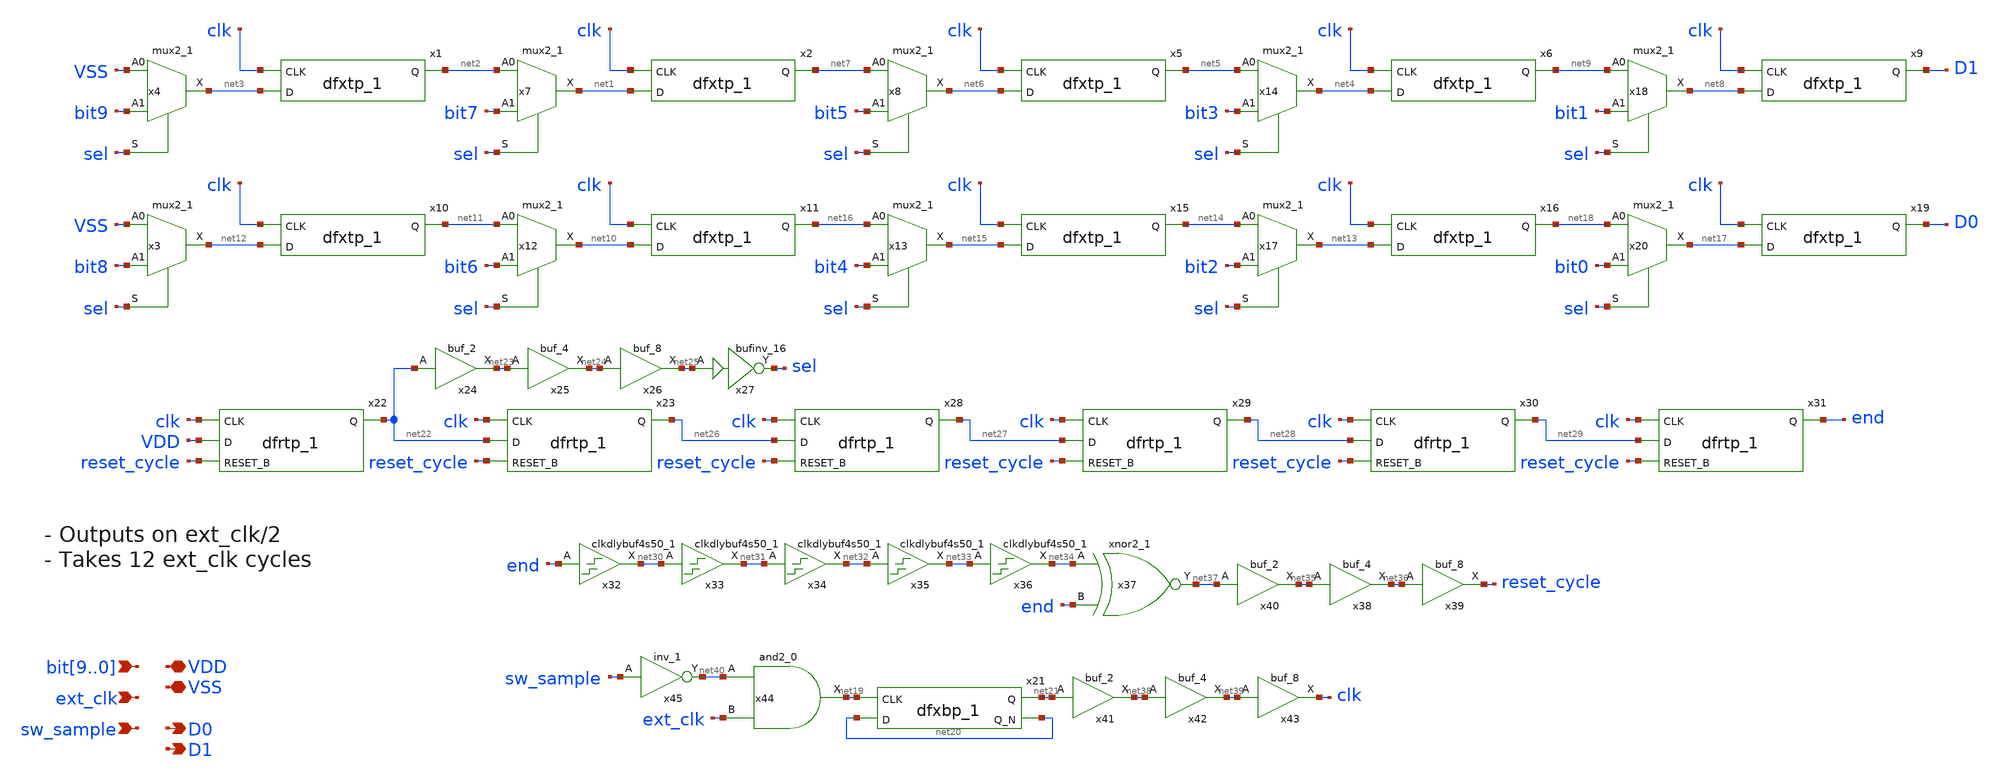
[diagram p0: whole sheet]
** sch_path: xschem/src/serializer/serializer.sch
**.subckt serializer bit9,bit8,bit7,bit6,bit5,bit4,bit3,bit2,bit1,bit0 VDD D0 VSS D1 ext_clk
*+ sw_sample
*.ipin bit9,bit8,bit7,bit6,bit5,bit4,bit3,bit2,bit1,bit0
*.iopin VDD
*.opin D0
*.iopin VSS
*.opin D1
*.ipin ext_clk
*.ipin sw_sample
x1 clk net3 VSS VSS VDD VDD net2 sky130_fd_sc_hd__dfxtp_1
x2 clk net1 VSS VSS VDD VDD net7 sky130_fd_sc_hd__dfxtp_1
x4 VSS bit9 sel VSS VSS VDD VDD net3 sky130_fd_sc_hd__mux2_1
x5 clk net6 VSS VSS VDD VDD net5 sky130_fd_sc_hd__dfxtp_1
x6 clk net4 VSS VSS VDD VDD net9 sky130_fd_sc_hd__dfxtp_1
x9 clk net8 VSS VSS VDD VDD D1 sky130_fd_sc_hd__dfxtp_1
x10 clk net12 VSS VSS VDD VDD net11 sky130_fd_sc_hd__dfxtp_1
x11 clk net10 VSS VSS VDD VDD net16 sky130_fd_sc_hd__dfxtp_1
x15 clk net15 VSS VSS VDD VDD net14 sky130_fd_sc_hd__dfxtp_1
x16 clk net13 VSS VSS VDD VDD net18 sky130_fd_sc_hd__dfxtp_1
x19 clk net17 VSS VSS VDD VDD D0 sky130_fd_sc_hd__dfxtp_1
x21 net19 net20 VSS VSS VDD VDD net21 net20 sky130_fd_sc_hd__dfxbp_1
x22 clk VDD reset_cycle VSS VSS VDD VDD net22 sky130_fd_sc_hd__dfrtp_1
x23 clk net22 reset_cycle VSS VSS VDD VDD net26 sky130_fd_sc_hd__dfrtp_1
x24 net22 VSS VSS VDD VDD net23 sky130_fd_sc_hd__buf_2
x25 net23 VSS VSS VDD VDD net24 sky130_fd_sc_hd__buf_4
x26 net24 VSS VSS VDD VDD net25 sky130_fd_sc_hd__buf_8
x27 net25 VSS VSS VDD VDD sel sky130_fd_sc_hd__bufinv_16
x28 clk net26 reset_cycle VSS VSS VDD VDD net27 sky130_fd_sc_hd__dfrtp_1
x29 clk net27 reset_cycle VSS VSS VDD VDD net28 sky130_fd_sc_hd__dfrtp_1
x30 clk net28 reset_cycle VSS VSS VDD VDD net29 sky130_fd_sc_hd__dfrtp_1
x31 clk net29 reset_cycle VSS VSS VDD VDD end sky130_fd_sc_hd__dfrtp_1
x32 end VSS VSS VDD VDD net30 sky130_fd_sc_hd__clkdlybuf4s50_1
x33 net30 VSS VSS VDD VDD net31 sky130_fd_sc_hd__clkdlybuf4s50_1
x34 net31 VSS VSS VDD VDD net32 sky130_fd_sc_hd__clkdlybuf4s50_1
x35 net32 VSS VSS VDD VDD net33 sky130_fd_sc_hd__clkdlybuf4s50_1
x36 net33 VSS VSS VDD VDD net34 sky130_fd_sc_hd__clkdlybuf4s50_1
x38 net35 VSS VSS VDD VDD net36 sky130_fd_sc_hd__buf_4
x39 net36 VSS VSS VDD VDD reset_cycle sky130_fd_sc_hd__buf_8
x40 net37 VSS VSS VDD VDD net35 sky130_fd_sc_hd__buf_2
x41 net21 VSS VSS VDD VDD net38 sky130_fd_sc_hd__buf_2
x42 net38 VSS VSS VDD VDD net39 sky130_fd_sc_hd__buf_4
x43 net39 VSS VSS VDD VDD clk sky130_fd_sc_hd__buf_8
x44 net40 ext_clk VSS VSS VDD VDD net19 sky130_fd_sc_hd__and2_0
x45 sw_sample VSS VSS VDD VDD net40 sky130_fd_sc_hd__inv_1
x3 VSS bit8 sel VSS VSS VDD VDD net12 sky130_fd_sc_hd__mux2_1
x7 net2 bit7 sel VSS VSS VDD VDD net1 sky130_fd_sc_hd__mux2_1
x8 net7 bit5 sel VSS VSS VDD VDD net6 sky130_fd_sc_hd__mux2_1
x12 net11 bit6 sel VSS VSS VDD VDD net10 sky130_fd_sc_hd__mux2_1
x13 net16 bit4 sel VSS VSS VDD VDD net15 sky130_fd_sc_hd__mux2_1
x14 net5 bit3 sel VSS VSS VDD VDD net4 sky130_fd_sc_hd__mux2_1
x17 net14 bit2 sel VSS VSS VDD VDD net13 sky130_fd_sc_hd__mux2_1
x18 net9 bit1 sel VSS VSS VDD VDD net8 sky130_fd_sc_hd__mux2_1
x20 net18 bit0 sel VSS VSS VDD VDD net17 sky130_fd_sc_hd__mux2_1
x37 net34 end VSS VSS VDD VDD net37 sky130_fd_sc_hd__xnor2_1
**.ends
.end
